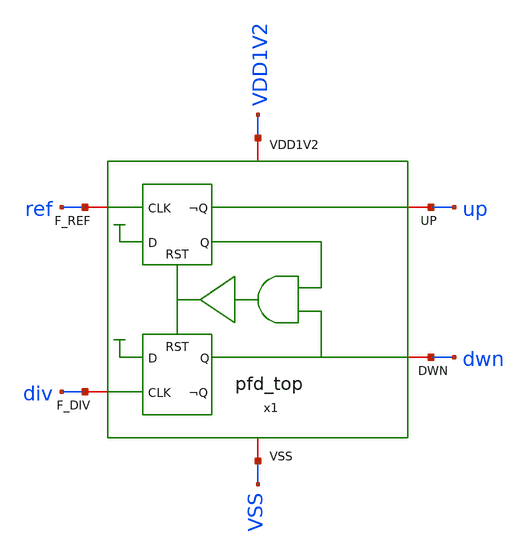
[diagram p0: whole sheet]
** sch_path: macros/pll_top/testbenches/xschem/pdf_tb.sch
* Copyright (C) 1998-2024 Stefan Frederik Schippers
* This program is free software; you can redistribute it and/or modify
* it under the terms of the GNU General Public License as published by
* the Free Software Foundation; either version 2 of the License, or
* (at your option) any later version.
* This program is distributed in the hope that it will be useful,
* but WITHOUT ANY WARRANTY; without even the implied warranty of
* MERCHANTABILITY or FITNESS FOR A PARTICULAR PURPOSE.  See the
* GNU General Public License for more details.
* You should have received a copy of the GNU General Public License
* along with this program; if not, write to the Free Software
**.subckt pdf_tb
x1 ref up dwn div VDD1V2 VSS pfd_top
**** begin user architecture code












**** end user architecture code
**.ends
.end
